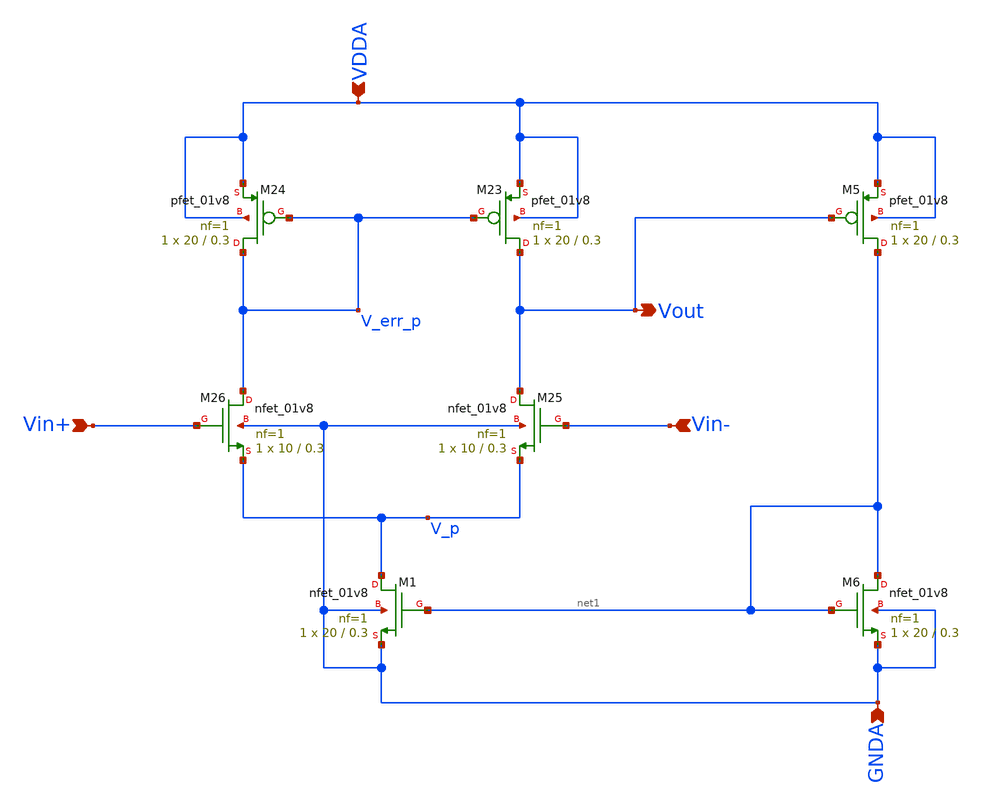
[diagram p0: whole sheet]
** sch_path: projects/bandgapref/xschem_ngspice/new_files/opamp_bandgap.sch
**.subckt opamp_bandgap Vin+ Vout Vin- GNDA VDDA
*.ipin Vin+
*.opin Vout
*.ipin Vin-
*.ipin GNDA
*.ipin VDDA
XM23 Vout V_err_p VDDA VDDA sky130_fd_pr__pfet_01v8 L=0.3 W=20 nf=1 ad='int((nf+1)/2) * W/nf * 0.29'
+ as='int((nf+2)/2) * W/nf * 0.29' pd='2*int((nf+1)/2) * (W/nf + 0.29)' ps='2*int((nf+2)/2) * (W/nf + 0.29)'
+ nrd='0.29 / W' nrs='0.29 / W' sa=0 sb=0 sd=0 mult=1 m=1
XM24 V_err_p V_err_p VDDA VDDA sky130_fd_pr__pfet_01v8 L=0.3 W=20 nf=1 ad='int((nf+1)/2) * W/nf * 0.29'
+ as='int((nf+2)/2) * W/nf * 0.29' pd='2*int((nf+1)/2) * (W/nf + 0.29)' ps='2*int((nf+2)/2) * (W/nf + 0.29)'
+ nrd='0.29 / W' nrs='0.29 / W' sa=0 sb=0 sd=0 mult=1 m=1
XM25 Vout Vin- V_p GNDA sky130_fd_pr__nfet_01v8 L=0.3 W=10 nf=1 ad='int((nf+1)/2) * W/nf * 0.29' as='int((nf+2)/2) * W/nf * 0.29'
+ pd='2*int((nf+1)/2) * (W/nf + 0.29)' ps='2*int((nf+2)/2) * (W/nf + 0.29)' nrd='0.29 / W' nrs='0.29 / W'
+ sa=0 sb=0 sd=0 mult=1 m=1
XM26 V_err_p Vin+ V_p GNDA sky130_fd_pr__nfet_01v8 L=0.3 W=10 nf=1 ad='int((nf+1)/2) * W/nf * 0.29' as='int((nf+2)/2) * W/nf * 0.29'
+ pd='2*int((nf+1)/2) * (W/nf + 0.29)' ps='2*int((nf+2)/2) * (W/nf + 0.29)' nrd='0.29 / W' nrs='0.29 / W'
+ sa=0 sb=0 sd=0 mult=1 m=1
XM1 V_p net1 GNDA GNDA sky130_fd_pr__nfet_01v8 L=0.3 W=20 nf=1 ad='int((nf+1)/2) * W/nf * 0.29' as='int((nf+2)/2) * W/nf * 0.29'
+ pd='2*int((nf+1)/2) * (W/nf + 0.29)' ps='2*int((nf+2)/2) * (W/nf + 0.29)' nrd='0.29 / W' nrs='0.29 / W'
+ sa=0 sb=0 sd=0 mult=1 m=1
XM5 net1 Vout VDDA VDDA sky130_fd_pr__pfet_01v8 L=0.3 W=20 nf=1 ad='int((nf+1)/2) * W/nf * 0.29' as='int((nf+2)/2) * W/nf * 0.29'
+ pd='2*int((nf+1)/2) * (W/nf + 0.29)' ps='2*int((nf+2)/2) * (W/nf + 0.29)' nrd='0.29 / W' nrs='0.29 / W'
+ sa=0 sb=0 sd=0 mult=1 m=1
XM6 net1 net1 GNDA GNDA sky130_fd_pr__nfet_01v8 L=0.3 W=20 nf=1 ad='int((nf+1)/2) * W/nf * 0.29' as='int((nf+2)/2) * W/nf * 0.29'
+ pd='2*int((nf+1)/2) * (W/nf + 0.29)' ps='2*int((nf+2)/2) * (W/nf + 0.29)' nrd='0.29 / W' nrs='0.29 / W'
+ sa=0 sb=0 sd=0 mult=1 m=1
**.ends
.end
